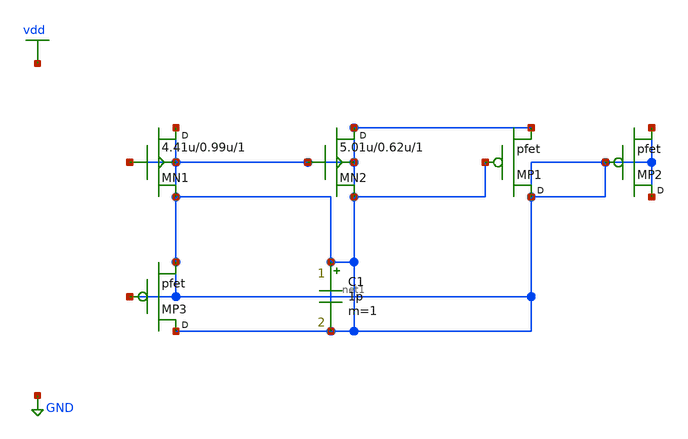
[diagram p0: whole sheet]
** sch_path: synthetic/generated/0020_synthetic.sch
**.subckt 0020_synthetic
MN1 net1 net1 net1 net1 nfet w=4.41u l=0.99u m=1
MN2 net1 net1 net1 net1 nfet w=5.01u l=0.62u m=1
MP1 net1 net1 net1 pfet m=1
MP2 net1 net1 net1 pfet m=1
MP3 net1 net1 net1 pfet m=1
C1 net1 net1 1p m=1
**.ends
.GLOBAL vdd
.GLOBAL GND
.end
